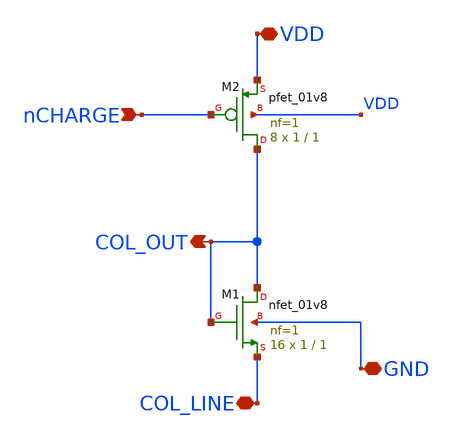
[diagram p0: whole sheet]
** sch_path: analog/xschem/col_amp_v2_std_dvs/xschem/col_amp.sch
**.subckt col_amp nCHARGE COL_OUT VDD GND COL_LINE
*.ipin nCHARGE
*.opin COL_OUT
*.iopin VDD
*.iopin GND
*.iopin COL_LINE
XM1 COL_OUT COL_OUT COL_LINE GND sky130_fd_pr__nfet_01v8 L=1 W=1 nf=1 ad='int((1 + 1)/2) * 1 / 1 * 0.29'
+ as='int((1 + 2)/2) * 1 / 1 * 0.29' pd='2*int((1 + 1)/2) * (1 / 1 + 0.29)' ps='2*int((1 + 2)/2) * (1 / 1 + 0.29)'
+ nrd='0.29 / 1 ' nrs='0.29 / 1 ' sa=0 sb=0 sd=0 mult=16 m=16
XM2 COL_OUT nCHARGE VDD VDD sky130_fd_pr__pfet_01v8 L=1 W=1 nf=1 ad='int((1 + 1)/2) * 1 / 1 * 0.29' as='int((1 + 2)/2) * 1 / 1 * 0.29'
+ pd='2*int((1 + 1)/2) * (1 / 1 + 0.29)' ps='2*int((1 + 2)/2) * (1 / 1 + 0.29)' nrd='0.29 / 1 ' nrs='0.29 / 1 '
+ sa=0 sb=0 sd=0 mult=8 m=8
**.ends
.end
